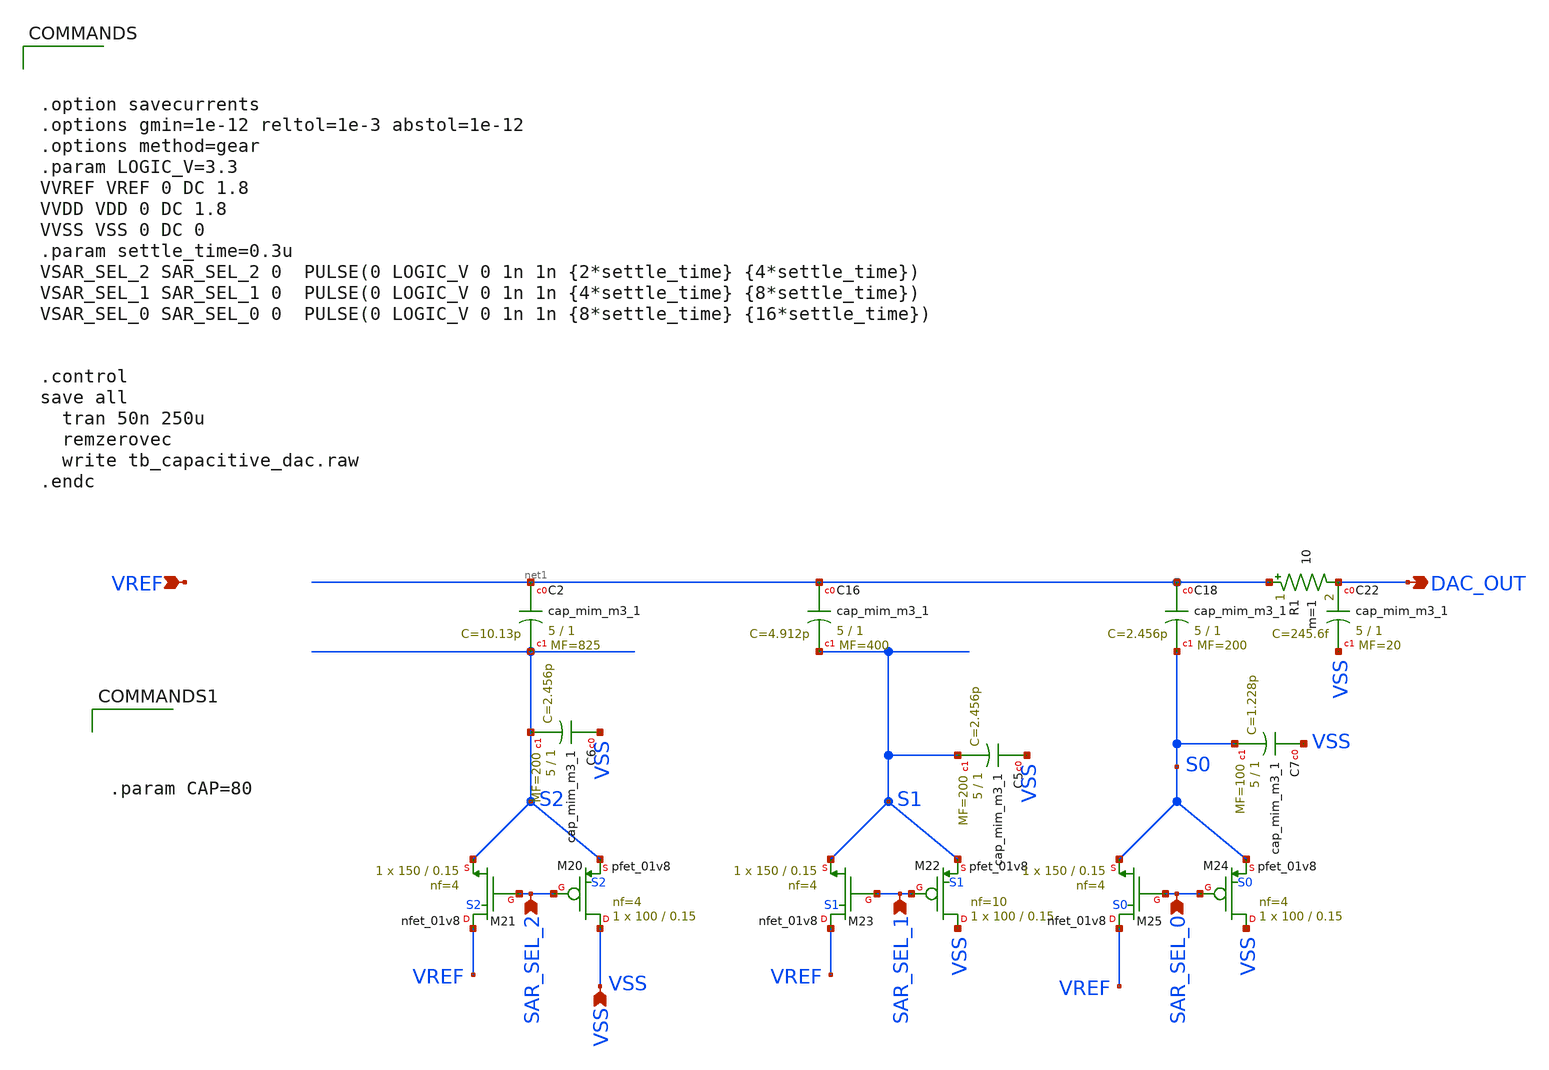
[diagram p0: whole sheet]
** sch_path: 3bit_sar_adc/tb_capacitive_dac.sch
**.subckt tb_capacitive_dac DAC_OUT SAR_SEL_1 SAR_SEL_0 SAR_SEL_2 VREF VSS
*.opin DAC_OUT
*.ipin SAR_SEL_1
*.ipin SAR_SEL_0
*.ipin SAR_SEL_2
*.ipin VREF
*.ipin VSS
XM20 VSS SAR_SEL_2 S2 S2 sky130_fd_pr__pfet_01v8 L=0.15 W=100 nf=4 ad='int((nf+1)/2) * W/nf * 0.29' as='int((nf+2)/2) * W/nf * 0.29'
+ pd='2*int((nf+1)/2) * (W/nf + 0.29)' ps='2*int((nf+2)/2) * (W/nf + 0.29)' nrd='0.29 / W' nrs='0.29 / W'
+ sa=0 sb=0 sd=0 mult=1 m=1
XM21 VREF SAR_SEL_2 S2 S2 sky130_fd_pr__nfet_01v8 L=0.15 W=150 nf=4 ad='int((nf+1)/2) * W/nf * 0.29'
+ as='int((nf+2)/2) * W/nf * 0.29' pd='2*int((nf+1)/2) * (W/nf + 0.29)' ps='2*int((nf+2)/2) * (W/nf + 0.29)'
+ nrd='0.29 / W' nrs='0.29 / W' sa=0 sb=0 sd=0 mult=1 m=1
XC16 net1 S1 sky130_fd_pr__cap_mim_m3_1 W=5 L=1 MF=400 m=400
XC18 net1 S0 sky130_fd_pr__cap_mim_m3_1 W=5 L=1 MF=200 m=200
XM22 VSS SAR_SEL_1 S1 S1 sky130_fd_pr__pfet_01v8 L=0.15 W=100 nf=10 ad='int((nf+1)/2) * W/nf * 0.29'
+ as='int((nf+2)/2) * W/nf * 0.29' pd='2*int((nf+1)/2) * (W/nf + 0.29)' ps='2*int((nf+2)/2) * (W/nf + 0.29)'
+ nrd='0.29 / W' nrs='0.29 / W' sa=0 sb=0 sd=0 mult=1 m=1
XM23 VREF SAR_SEL_1 S1 S1 sky130_fd_pr__nfet_01v8 L=0.15 W=150 nf=4 ad='int((nf+1)/2) * W/nf * 0.29'
+ as='int((nf+2)/2) * W/nf * 0.29' pd='2*int((nf+1)/2) * (W/nf + 0.29)' ps='2*int((nf+2)/2) * (W/nf + 0.29)'
+ nrd='0.29 / W' nrs='0.29 / W' sa=0 sb=0 sd=0 mult=1 m=1
XM24 VSS SAR_SEL_0 S0 S0 sky130_fd_pr__pfet_01v8 L=0.15 W=100 nf=4 ad='int((nf+1)/2) * W/nf * 0.29' as='int((nf+2)/2) * W/nf * 0.29'
+ pd='2*int((nf+1)/2) * (W/nf + 0.29)' ps='2*int((nf+2)/2) * (W/nf + 0.29)' nrd='0.29 / W' nrs='0.29 / W'
+ sa=0 sb=0 sd=0 mult=1 m=1
XM25 VREF SAR_SEL_0 S0 S0 sky130_fd_pr__nfet_01v8 L=0.15 W=150 nf=4 ad='int((nf+1)/2) * W/nf * 0.29'
+ as='int((nf+2)/2) * W/nf * 0.29' pd='2*int((nf+1)/2) * (W/nf + 0.29)' ps='2*int((nf+2)/2) * (W/nf + 0.29)'
+ nrd='0.29 / W' nrs='0.29 / W' sa=0 sb=0 sd=0 mult=1 m=1
XC22 DAC_OUT VSS sky130_fd_pr__cap_mim_m3_1 W=5 L=1 MF=20 m=20
XC2 net1 S2 sky130_fd_pr__cap_mim_m3_1 W=5 L=1 MF=825 m=825
XC6 VSS S2 sky130_fd_pr__cap_mim_m3_1 W=5 L=1 MF=200 m=200
XC5 VSS S1 sky130_fd_pr__cap_mim_m3_1 W=5 L=1 MF=200 m=200
XC7 VSS S0 sky130_fd_pr__cap_mim_m3_1 W=5 L=1 MF=100 m=100
R1 net1 DAC_OUT 10 m=1
**** begin user architecture code

** opencircuitdesign pdks install
.lib $::SKYWATER_MODELS/sky130.lib.spice tt
.include $::SKYWATER_STDCELLS/sky130_fd_sc_hd.spice
.include /foss/pdks/sky130A/libs.tech/xschem/sky130_stdcells/




.option savecurrents
.options gmin=1e-12 reltol=1e-3 abstol=1e-12
.options method=gear
.param LOGIC_V=3.3
VVREF VREF 0 DC 1.8
VVDD VDD 0 DC 1.8
VVSS VSS 0 DC 0
.param settle_time=0.3u
VSAR_SEL_2 SAR_SEL_2 0  PULSE(0 LOGIC_V 0 1n 1n {2*settle_time} {4*settle_time})
VSAR_SEL_1 SAR_SEL_1 0  PULSE(0 LOGIC_V 0 1n 1n {4*settle_time} {8*settle_time})
VSAR_SEL_0 SAR_SEL_0 0  PULSE(0 LOGIC_V 0 1n 1n {8*settle_time} {16*settle_time})


.control
save all
  tran 50n 250u
  remzerovec
  write tb_capacitive_dac.raw
.endc






.param CAP=80



**** end user architecture code
**.ends
.end
